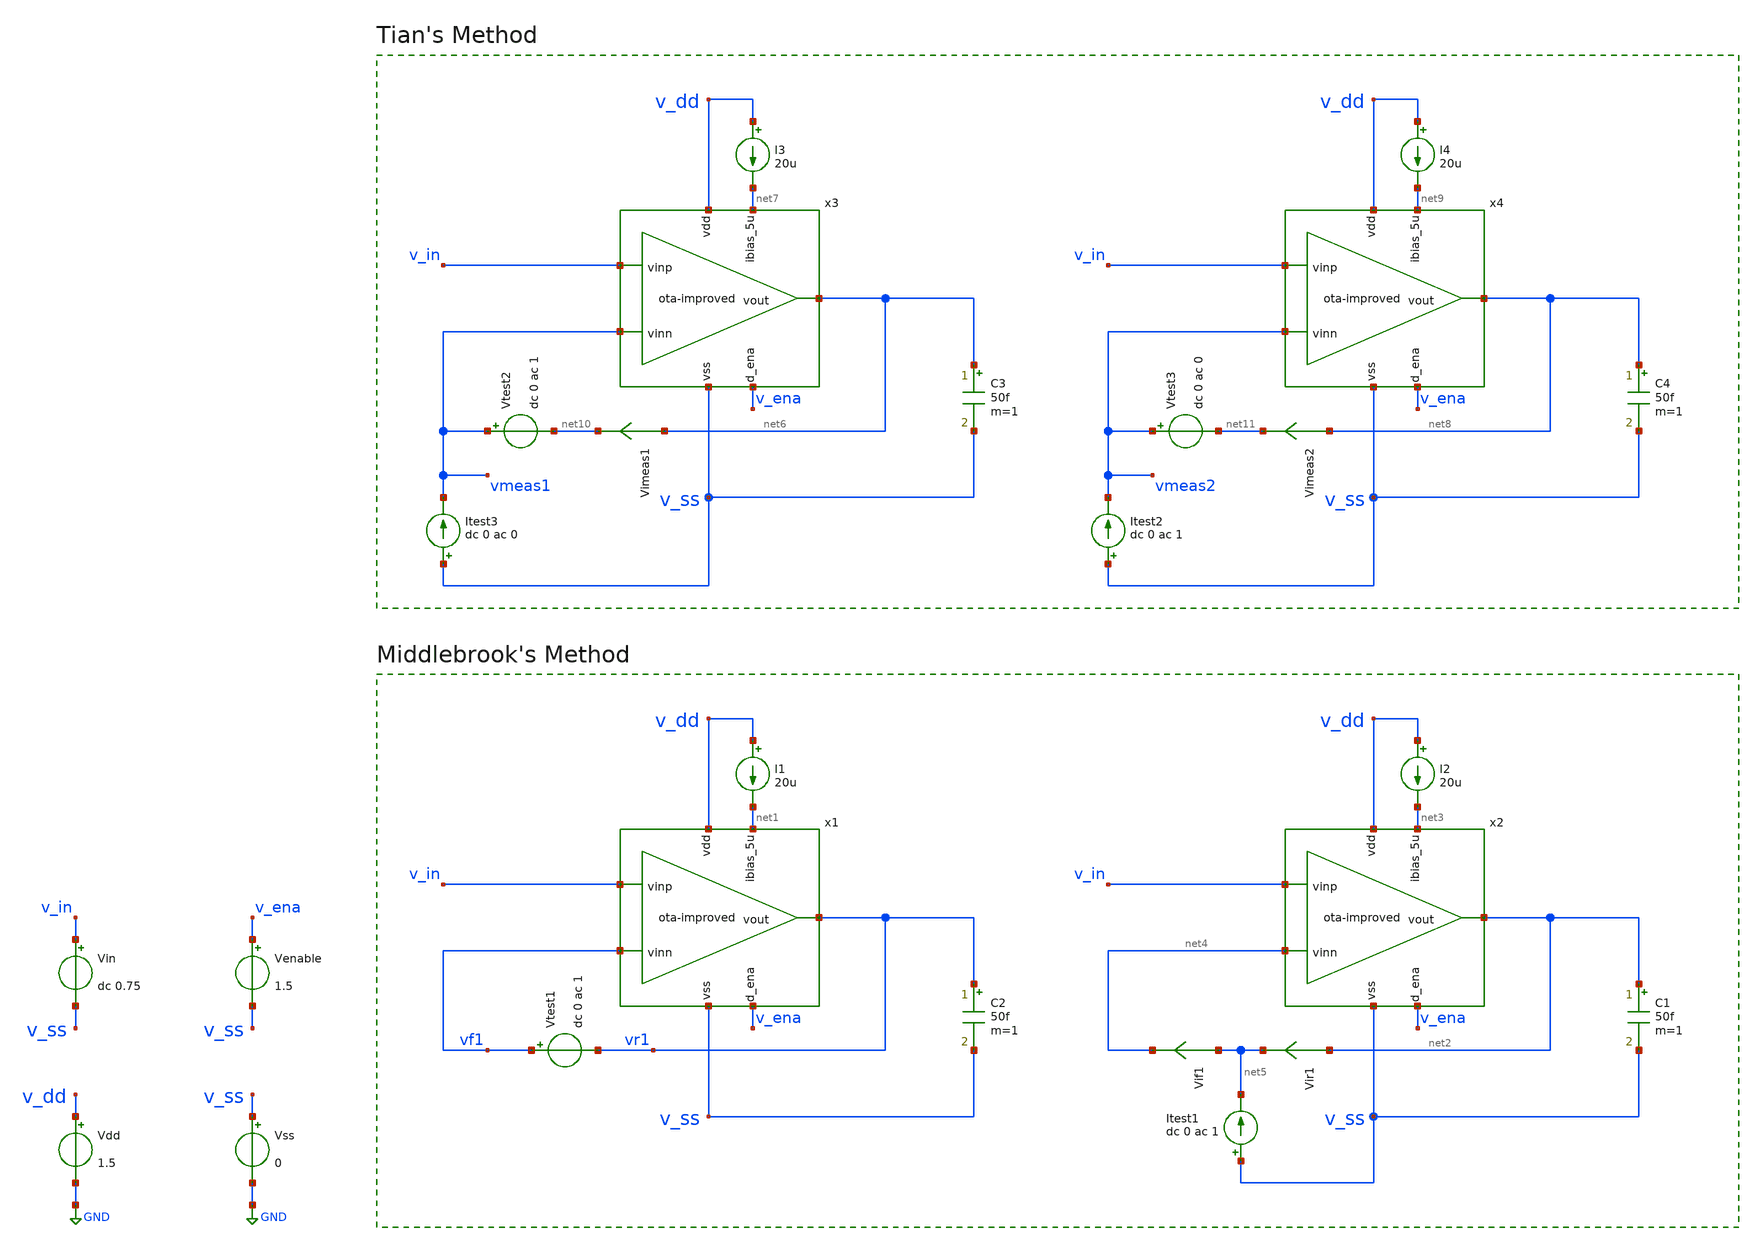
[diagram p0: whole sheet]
** sch_path: xschem/ota-improved_tb-loopgain.sch
* (c) 2024-2025 H. Pretl, S. Dorrer, Apache-2.0 license
* xschem/ota-improved.sch:
* (c) 2024-2025 Harald Pretl, Apache-2.0 license
**.subckt ota-improved_tb-loopgain
Vdd v_dd GND 1.5
Vss v_ss GND 0
Vin v_in v_ss dc 0.75
Venable v_ena v_ss 1.5
C2 vr1 v_ss 50f m=1
I1 v_dd net1 20u
Vtest1 vf1 vr1 dc 0 ac 1
C1 net2 v_ss 50f m=1
I2 v_dd net3 20u
Vir1 net2 net5 0
.save i(vir1)
Vif1 net5 net4 0
.save i(vif1)
Itest1 v_ss net5 dc 0 ac 1
C3 net6 v_ss 50f m=1
I3 v_dd net7 20u
C4 net8 v_ss 50f m=1
I4 v_dd net9 20u
Itest3 v_ss vmeas1 dc 0 ac 0
Vtest2 vmeas1 net10 dc 0 ac 1
Vimeas1 net6 net10 0
.save i(vimeas1)
Itest2 v_ss vmeas2 dc 0 ac 1
Vtest3 vmeas2 net11 dc 0 ac 0
Vimeas2 net8 net11 0
.save i(vimeas2)
x1 v_dd vr1 v_in vf1 net1 v_ena v_ss ota-improved
x2 v_dd net2 v_in net4 net3 v_ena v_ss ota-improved
x3 v_dd net6 v_in vmeas1 net7 v_ena v_ss ota-improved
x4 v_dd net8 v_in vmeas2 net9 v_ena v_ss ota-improved
**** begin user architecture code

.lib cornerMOSlv.lib mos_tt
.lib cornerRES.lib res_typ



.param temp=27
.options savecurrents reltol=1e-3 abstol=1e-12 gmin=1e-15
.control
save all

* Operating Point Analysis
op
remzerovec
write ota-improved_tb-loopgain.raw
set appendwrite

* AC Analysis
ac dec 101 1 100G
remzerovec
write ota-improved_tb-loopgain.raw
set appendwrite

* Middlebrook's Method
let tv=-v(vr1)/v(vf1)
let ti=-i(vir1)/i(vif1)
let tmb=(tv*ti - 1)/(tv + ti + 2)

plot db(tmb) ylabel 'Magnitude - Middlebrook'
plot 180/pi*cphase(tmb) ylabel 'Phase - Middlebrook'

* Tian's Method
* vtest=0, itest=1:
let A=i(Vimeas2)
let C=v(vmeas2)

* vtest=1, itest=0:
let B=i(Vimeas1)
let D=v(vmeas1)
let ttian=(A*D-B*C-A)/(2*(B*C-A*D)+A-D+1)

plot db(ttian) ylabel 'Magnitude - Tian'
plot 180/pi*cphase(ttian) ylabel 'Phase - Tian'

* Middlebrook vs. Tian
plot db(tmb) db(ttian) ylabel 'Magnitude'
plot 180/pi*cphase(tmb) 180/pi*cphase(ttian) ylabel 'Phase'

write ota-improved_tb-loopgain.raw

*quit
.endc


**** end user architecture code
**.ends

* expanding   symbol:  ota-improved.sym # of pins=7
** sym_path: xschem/ota-improved.sym
** sch_path: xschem/ota-improved.sch
.subckt ota-improved vdd vout vinp vinn ibias_5u d_ena vss
*.ipin ibias_5u
*.iopin vdd
*.iopin vss
*.ipin vinp
*.ipin vinn
*.opin vout
*.ipin d_ena
XM5 net7 gate vss vss sg13_lv_nmos w=6u l=5u ng=3 m=1 mm_ok=1
XM4 net2 gate_p vdd vdd sg13_lv_pmos w=3u l=0.5u ng=1 m=1 mm_ok=1
XM1 net5 vinp tail vss sg13_lv_nmos w=1u l=0.5u ng=1 m=1 mm_ok=1
XM2 net6 vinn tail vss sg13_lv_nmos w=1u l=0.5u ng=1 m=1 mm_ok=1
XM3 net3 gate_p vdd vdd sg13_lv_pmos w=3u l=0.5u ng=1 m=1 mm_ok=1
XM6 net1 gate vss vss sg13_lv_nmos w=2u l=5u ng=1 m=1 mm_ok=1
XMpd5 gate ena_n vss vss sg13_lv_nmos w=1u l=0.13u ng=1 m=1 mm_ok=1
XMpd3 ena ena_n vss vss sg13_lv_nmos w=1u l=0.13u ng=1 m=1 mm_ok=1
XMpd4 ena ena_n vdd vdd sg13_lv_pmos w=1u l=0.13u ng=1 m=1 mm_ok=1
XMpd6 net1 ena gate vss sg13_lv_nmos w=1u l=0.13u ng=1 m=1 mm_ok=1
XM2c vout dp_casc net6 vss sg13_lv_nmos w=1u l=0.5u ng=1 m=1 mm_ok=1
XM1c gate_p dp_casc net5 vss sg13_lv_nmos w=1u l=0.5u ng=1 m=1 mm_ok=1
XM4c vout gate_pc net2 vdd sg13_lv_pmos w=3u l=0.5u ng=1 m=1 mm_ok=1
XM3c gate_p gate_pc net3 vdd sg13_lv_pmos w=3u l=0.5u ng=1 m=1 mm_ok=1
XM7 net4 gate vss vss sg13_lv_nmos w=2u l=5u ng=1 m=1 mm_ok=1
XMpd8 gate_p ena vdd vdd sg13_lv_pmos w=1u l=0.13u ng=1 m=1 mm_ok=1
XM8_1 net8 gate_pc vdd vdd sg13_lv_pmos w=3u l=0.5u ng=1 m=1 mm_ok=1
XM9_1 net9 gate_pc vdd vdd sg13_lv_pmos w=3u l=0.5u ng=1 m=1 mm_ok=1
XMpd7 gate_pc ena vdd vdd sg13_lv_pmos w=1u l=0.13u ng=1 m=1 mm_ok=1
XM10_3 net10 dp_casc net11 vss sg13_lv_nmos w=1u l=0.5u ng=1 m=1 mm_ok=1
Vmeas gate_pc net4 0
.save i(vmeas)
Vmeas1 tail net7 0
.save i(vmeas1)
XMpd1 ena_n d_ena vss vss sg13_lv_nmos w=1u l=0.13u ng=1 m=1 mm_ok=1
XMpd2 ena_n d_ena vdd vdd sg13_lv_pmos w=1u l=0.13u ng=1 m=1 mm_ok=1
Vmeas4 ibias_5u net1 0
.save i(vmeas4)
XMpd11 vout ena_n vss vss sg13_lv_nmos w=0.5u l=0.13u ng=1 m=1 mm_ok=1
XM10_4 net11 dp_casc tail vss sg13_lv_nmos w=1u l=0.5u ng=1 m=1 mm_ok=1
XMdecoup1 vss gate vss vss sg13_lv_nmos w=8u l=1u ng=4 m=1 mm_ok=1
XMdecoup3 vdd gate_pc vdd vdd sg13_lv_pmos w=12u l=0.5u ng=4 m=1 mm_ok=1
XM10_2 net12 dp_casc net10 vss sg13_lv_nmos w=1u l=0.5u ng=1 m=1 mm_ok=1
XM10_1 dp_casc dp_casc net12 vss sg13_lv_nmos w=1u l=0.5u ng=1 m=1 mm_ok=1
XM8_2 net13 gate_pc net8 vdd sg13_lv_pmos w=3u l=0.5u ng=1 m=1 mm_ok=1
XM8_3 net14 gate_pc net13 vdd sg13_lv_pmos w=3u l=0.5u ng=1 m=1 mm_ok=1
XM9_2 net15 gate_pc net9 vdd sg13_lv_pmos w=3u l=0.5u ng=1 m=1 mm_ok=1
XM9_3 net16 gate_pc net15 vdd sg13_lv_pmos w=3u l=0.5u ng=1 m=1 mm_ok=1
XM8_4 gate_pc gate_pc net14 vdd sg13_lv_pmos w=3u l=0.5u ng=1 m=1 mm_ok=1
XM9_4 dp_casc gate_pc net16 vdd sg13_lv_pmos w=3u l=0.5u ng=1 m=1 mm_ok=1
.ends

.GLOBAL GND
.end
